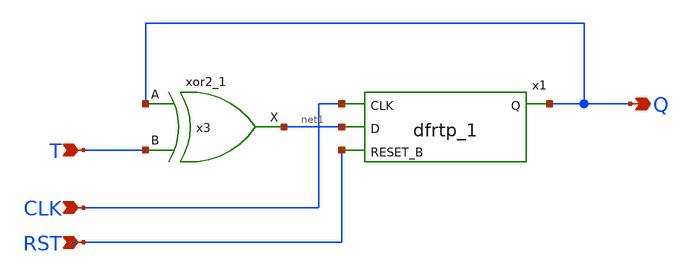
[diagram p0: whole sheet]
** sch_path: xschem/T_flip_flop/asyn_rst_.sch
**.subckt asyn_rst_ T CLK Q RST
*.ipin T
*.ipin CLK
*.opin Q
*.ipin RST
x1 CLK net1 RST GND GND VDD VDD Q sky130_fd_sc_lp__dfrtp_1
x3 Q T GND GND VDD VDD net1 sky130_fd_sc_lp__xor2_1
**.ends
.end
